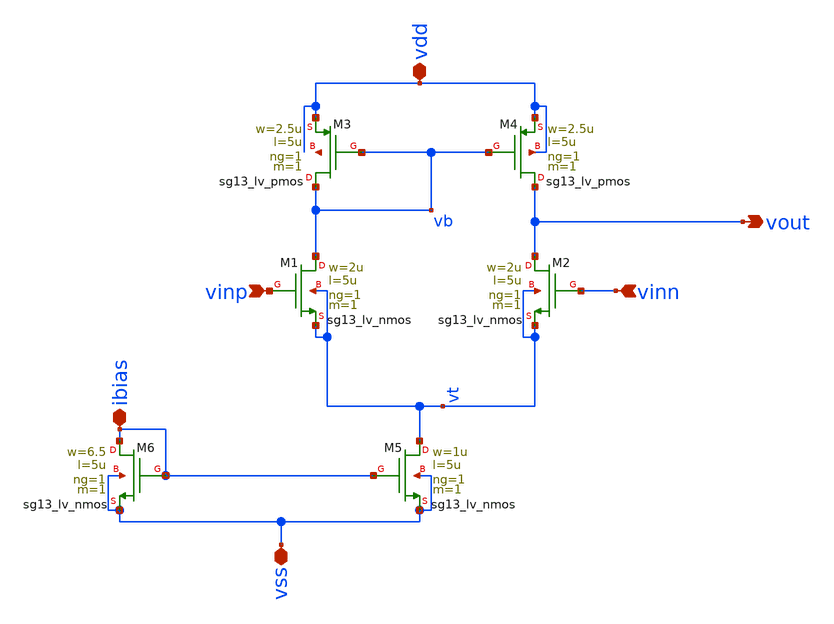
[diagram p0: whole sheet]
** sch_path: 004_Real_Circuits/5T-OTA.sch
**.subckt 5T-OTA vinp vdd vss vout vinn ibias
*.ipin vinp
*.iopin vdd
*.iopin vss
*.opin vout
*.ipin vinn
*.iopin ibias
XM1 vb vinp vt vt sg13_lv_nmos w=2u l=5u ng=1 m=1 mm_ok=1
XM5 vt ibias vss vss sg13_lv_nmos w=1u l=5u ng=1 m=1 mm_ok=1
XM2 vout vinn vt vt sg13_lv_nmos w=2u l=5u ng=1 m=1 mm_ok=1
XM6 ibias ibias vss vss sg13_lv_nmos w=6.5 l=5u ng=1 m=1 mm_ok=1
XM3 vb vb vdd net1 sg13_lv_pmos w=2.5u l=5u ng=1 m=1 mm_ok=1
XM4 vout vb vdd vdd sg13_lv_pmos w=2.5u l=5u ng=1 m=1 mm_ok=1
**.ends
.end
